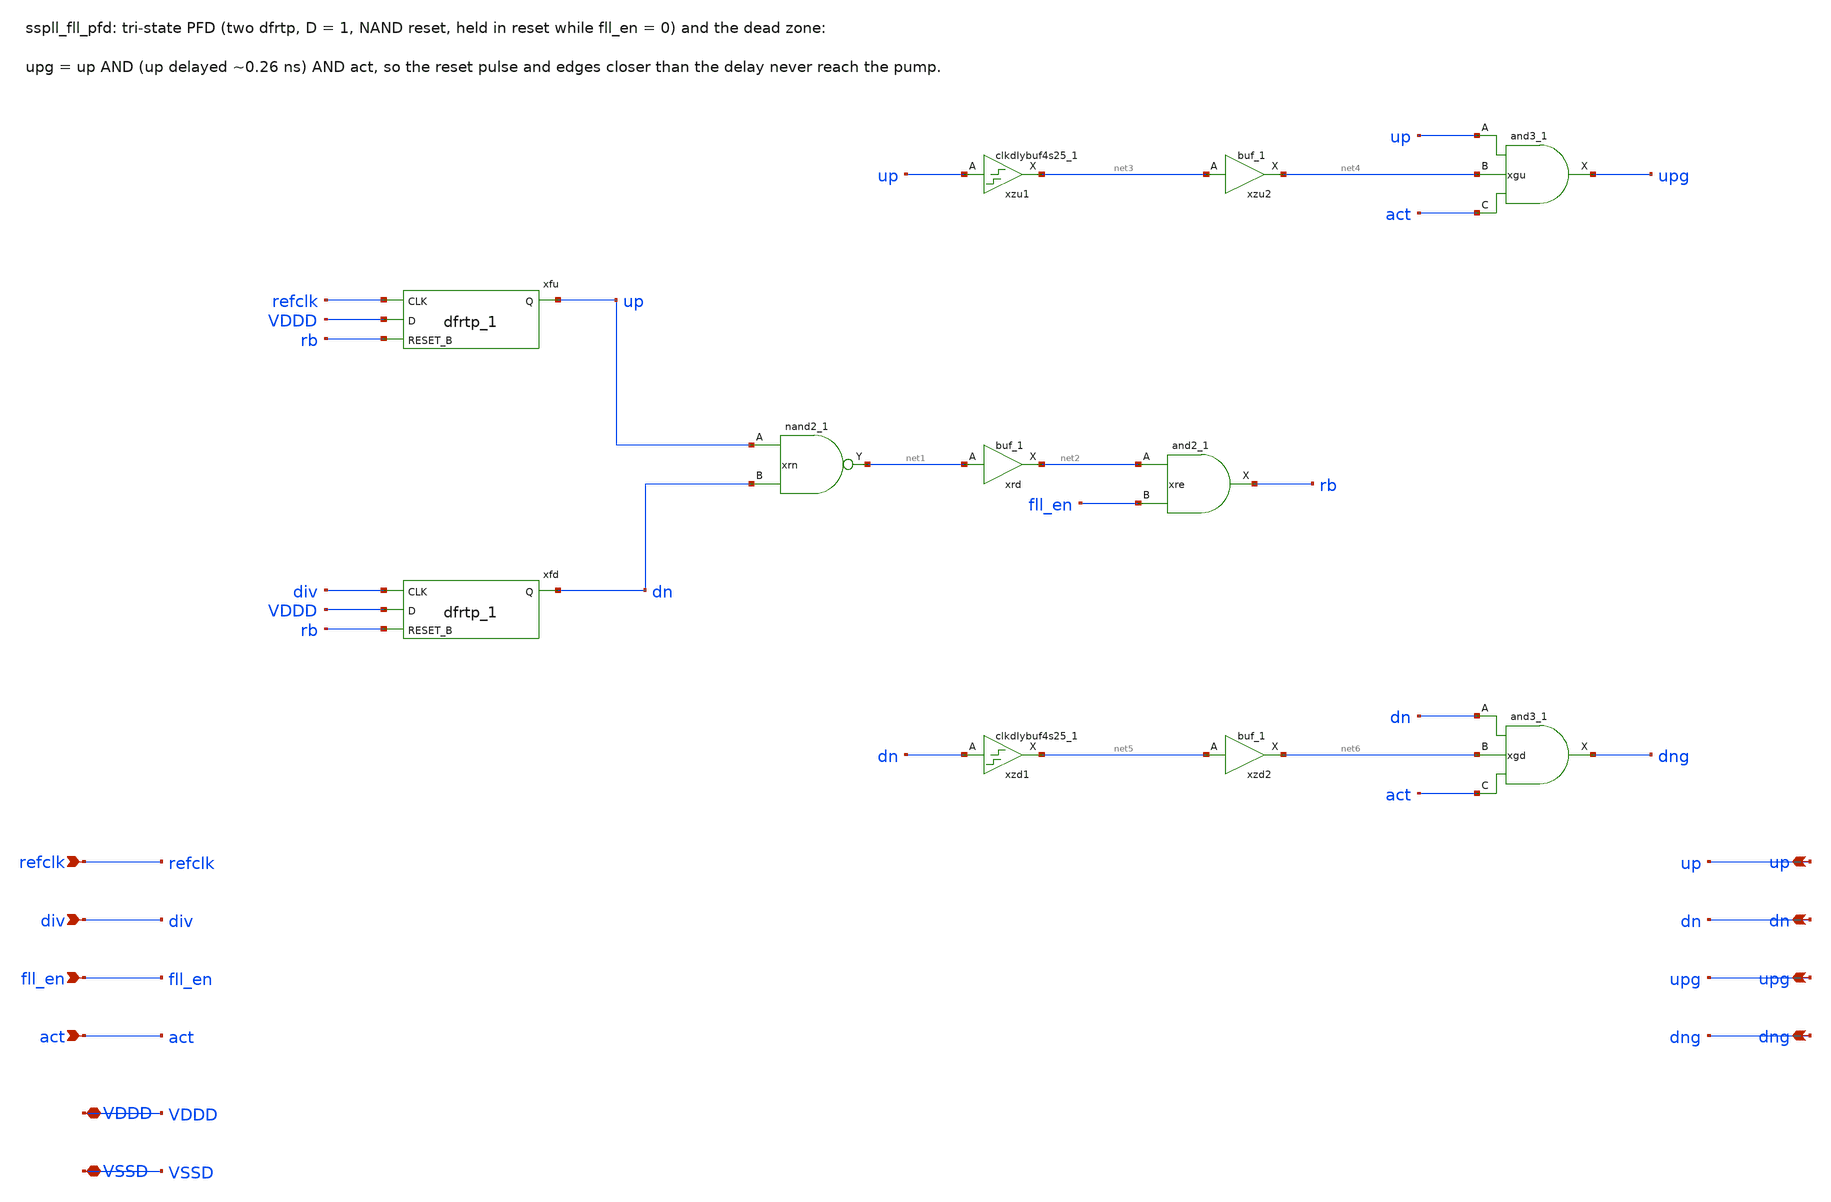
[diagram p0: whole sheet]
** sch_path: xschem/fll_hv/sspll_fll_pfd.sch
**.subckt sspll_fll_pfd refclk div fll_en act up dn upg dng VDDD VSSD
*.ipin refclk
*.ipin div
*.ipin fll_en
*.ipin act
*.opin up
*.opin dn
*.opin upg
*.opin dng
*.iopin VDDD
*.iopin VSSD
xfu refclk VDDD rb VSSD VSSD VDDD VDDD up sky130_fd_sc_hd__dfrtp_1
xfd div VDDD rb VSSD VSSD VDDD VDDD dn sky130_fd_sc_hd__dfrtp_1
xrn up dn VSSD VSSD VDDD VDDD net1 sky130_fd_sc_hd__nand2_1
xrd net1 VSSD VSSD VDDD VDDD net2 sky130_fd_sc_hd__buf_1
xre net2 fll_en VSSD VSSD VDDD VDDD rb sky130_fd_sc_hd__and2_1
xzu1 up VSSD VSSD VDDD VDDD net3 sky130_fd_sc_hd__clkdlybuf4s25_1
xzu2 net3 VSSD VSSD VDDD VDDD net4 sky130_fd_sc_hd__buf_1
xgu up net4 act VSSD VSSD VDDD VDDD upg sky130_fd_sc_hd__and3_1
xzd1 dn VSSD VSSD VDDD VDDD net5 sky130_fd_sc_hd__clkdlybuf4s25_1
xzd2 net5 VSSD VSSD VDDD VDDD net6 sky130_fd_sc_hd__buf_1
xgd dn net6 act VSSD VSSD VDDD VDDD dng sky130_fd_sc_hd__and3_1
**.ends
.end
